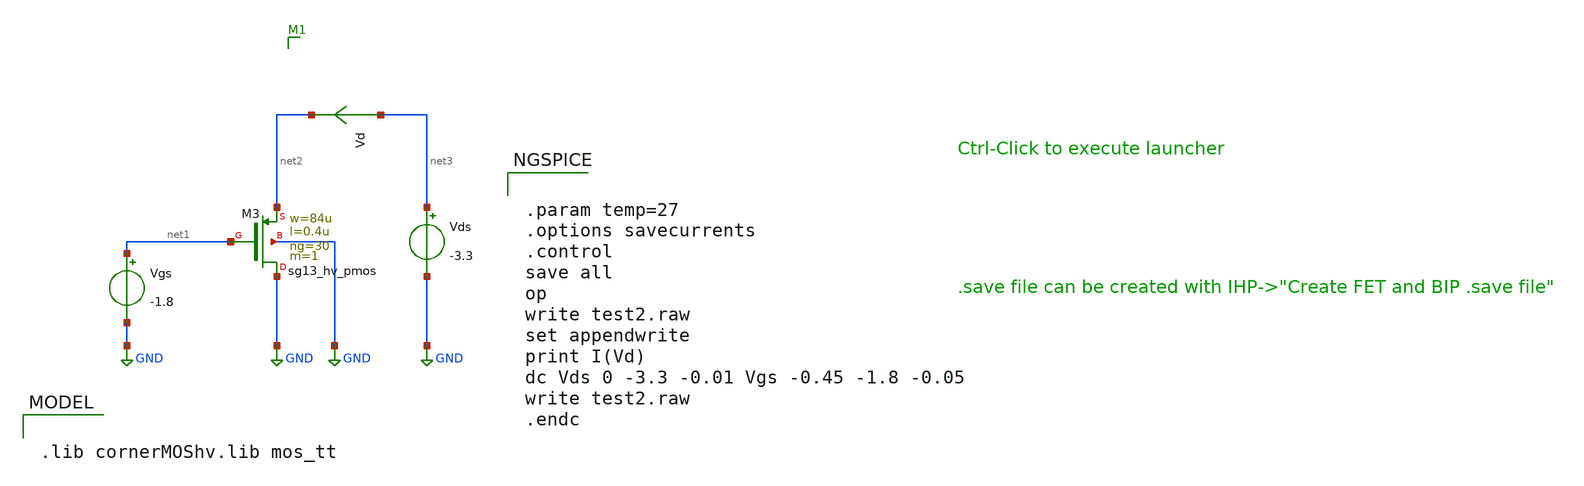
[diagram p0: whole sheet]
** sch_path: schematic/test2.sch
**.subckt test2
Vgs net1 GND -1.8
Vds net3 GND -3.3
Vd net3 net2 0
.save i(vd)
XM3 GND net1 net2 GND sg13_hv_pmos w=84u l=0.4u ng=30 m=1 mm_ok=1
**** begin user architecture code

.lib cornerMOShv.lib mos_tt



.param temp=27
.options savecurrents
.control
save all
op
write test2.raw
set appendwrite
print I(Vd)
dc Vds 0 -3.3 -0.01 Vgs -0.45 -1.8 -0.05
write test2.raw
.endc


**** end user architecture code
**.ends
.GLOBAL GND
.end
